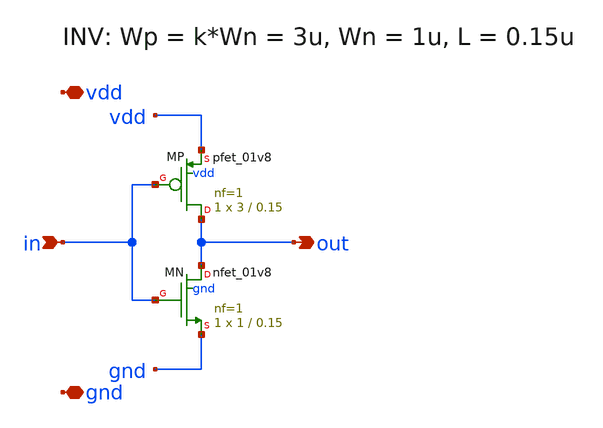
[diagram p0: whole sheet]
** sch_path: proj/xschem/inv.sch
**.subckt inv in out vdd gnd
*.ipin in
*.opin out
*.iopin vdd
*.iopin gnd
XMP out in vdd vdd sky130_fd_pr__pfet_01v8 L=0.15 W=3 nf=1 ad='int((1 + 1)/2) * 3 / 1 * 0.29' as='int((1 + 2)/2) * 3 / 1 * 0.29'
+ pd='2*int((1 + 1)/2) * (3 / 1 + 0.29)' ps='2*int((1 + 2)/2) * (3 / 1 + 0.29)' nrd='0.29 / 3 ' nrs='0.29 / 3 '
+ sa=0 sb=0 sd=0 mult=1 m=1
XMN out in gnd gnd sky130_fd_pr__nfet_01v8 L=0.15 W=1 nf=1 ad='int((nf+1)/2) * W/nf * 0.29' as='int((nf+2)/2) * W/nf * 0.29'
+ pd='2*int((nf+1)/2) * (W/nf + 0.29)' ps='2*int((nf+2)/2) * (W/nf + 0.29)' nrd='0.29 / W' nrs='0.29 / W'
+ sa=0 sb=0 sd=0 mult=1 m=1
**.ends
.end
